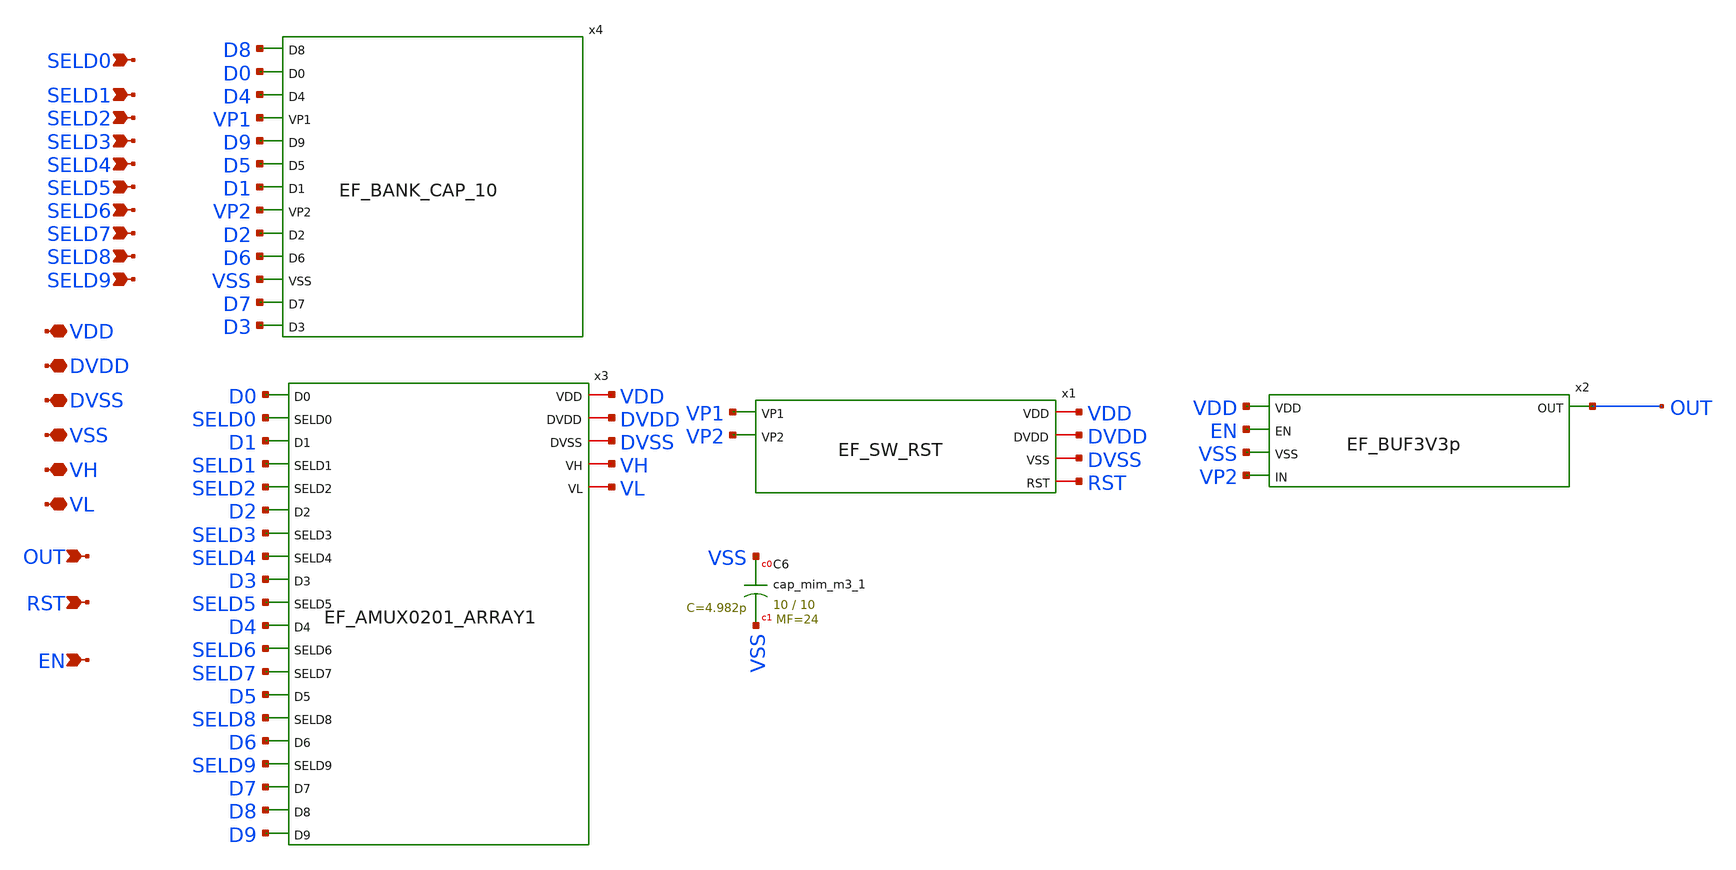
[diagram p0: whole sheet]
** sch_path: spice/xschem/EF_DACSCA1001.sch
**.subckt EF_DACSCA1001 SELD0 SELD1 SELD2 SELD3 SELD4 SELD5 SELD6 SELD7 SELD8 SELD9 VDD DVDD DVSS VH
*+ VL VSS OUT RST EN
*.ipin SELD0
*.ipin SELD1
*.ipin SELD2
*.ipin SELD3
*.ipin SELD4
*.ipin SELD5
*.ipin SELD6
*.ipin SELD7
*.ipin SELD8
*.ipin SELD9
*.iopin VDD
*.iopin DVDD
*.iopin DVSS
*.iopin VH
*.iopin VL
*.iopin VSS
*.ipin OUT
*.ipin RST
*.ipin EN
x4 D8 D0 D4 VP1 D9 D5 D1 VP2 D2 D6 VSS D7 D3 EF_BANK_CAP_10
x3 D0 SELD0 D1 SELD1 SELD2 D2 SELD3 SELD4 D3 SELD5 D4 SELD6 SELD7 D5 SELD8 D6 SELD9 D7 D8 D9 VDD
+ DVDD DVSS VH VL EF_AMUX0201_ARRAY1
x1 VP1 VP2 VDD DVDD DVSS RST EF_SW_RST
x2 VDD OUT EN VSS VP2 EF_BUF3V3p
XC6 VSS VSS sky130_fd_pr__cap_mim_m3_1 W=10 L=10 MF=24 m=24
**.ends
.end
